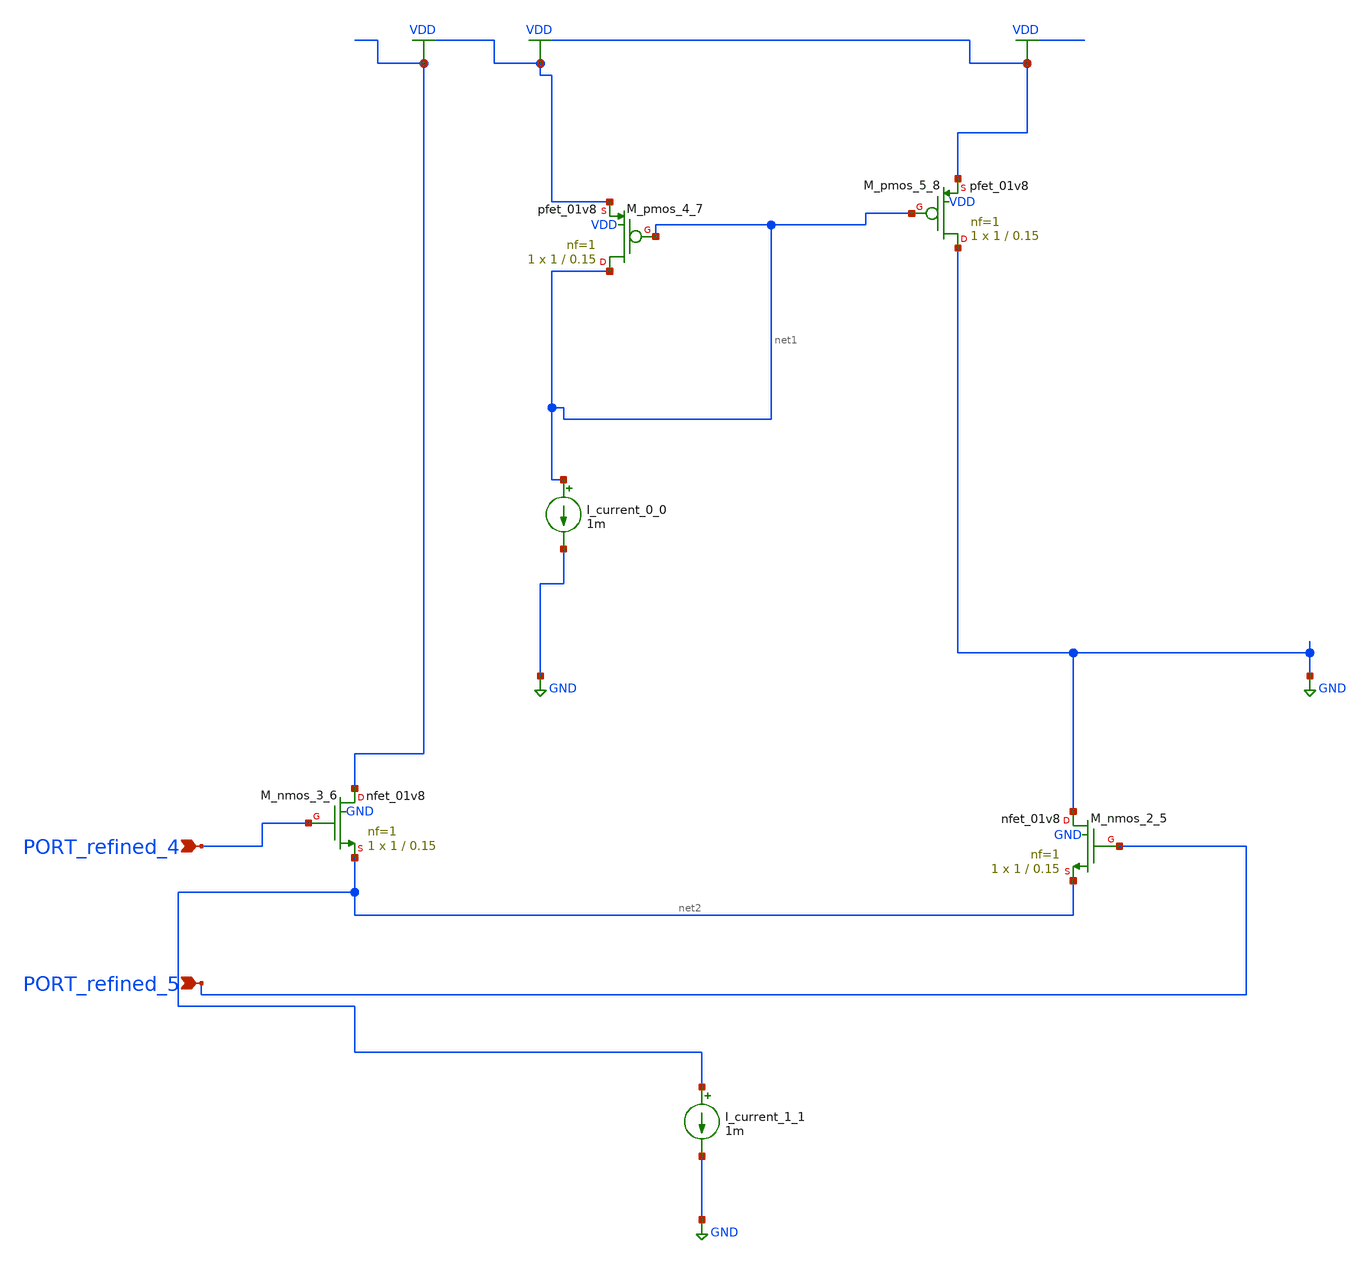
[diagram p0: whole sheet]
** sch_path: schematics/AMSNet/270.sch
**.subckt 270 PORT_refined_4 PORT_refined_5
*.ipin PORT_refined_4
*.ipin PORT_refined_5
I_current_0_0 net1 GND 1m
I_current_1_1 net2 GND 1m
XM_nmos_2_5 GND PORT_refined_5 net2 GND sky130_fd_pr__nfet_01v8 L=0.15 W=1 nf=1 ad='int((1 + 1)/2) * 1 / 1 * 0.29'
+ as='int((1 + 2)/2) * 1 / 1 * 0.29' pd='2*int((1 + 1)/2) * (1 / 1 + 0.29)' ps='2*int((1 + 2)/2) * (1 / 1 + 0.29)'
+ nrd='0.29 / 1 ' nrs='0.29 / 1 ' sa=0 sb=0 sd=0 mult=1 m=1
XM_nmos_3_6 VDD PORT_refined_4 net2 GND sky130_fd_pr__nfet_01v8 L=0.15 W=1 nf=1 ad='int((1 + 1)/2) * 1 / 1 * 0.29'
+ as='int((1 + 2)/2) * 1 / 1 * 0.29' pd='2*int((1 + 1)/2) * (1 / 1 + 0.29)' ps='2*int((1 + 2)/2) * (1 / 1 + 0.29)'
+ nrd='0.29 / 1 ' nrs='0.29 / 1 ' sa=0 sb=0 sd=0 mult=1 m=1
XM_pmos_4_7 net1 net1 VDD VDD sky130_fd_pr__pfet_01v8 L=0.15 W=1 nf=1 ad='int((1 + 1)/2) * 1 / 1 * 0.29'
+ as='int((1 + 2)/2) * 1 / 1 * 0.29' pd='2*int((1 + 1)/2) * (1 / 1 + 0.29)' ps='2*int((1 + 2)/2) * (1 / 1 + 0.29)'
+ nrd='0.29 / 1 ' nrs='0.29 / 1 ' sa=0 sb=0 sd=0 mult=1 m=1
XM_pmos_5_8 GND net1 VDD VDD sky130_fd_pr__pfet_01v8 L=0.15 W=1 nf=1 ad='int((1 + 1)/2) * 1 / 1 * 0.29'
+ as='int((1 + 2)/2) * 1 / 1 * 0.29' pd='2*int((1 + 1)/2) * (1 / 1 + 0.29)' ps='2*int((1 + 2)/2) * (1 / 1 + 0.29)'
+ nrd='0.29 / 1 ' nrs='0.29 / 1 ' sa=0 sb=0 sd=0 mult=1 m=1
**.ends
.GLOBAL GND
.GLOBAL VDD
.end
